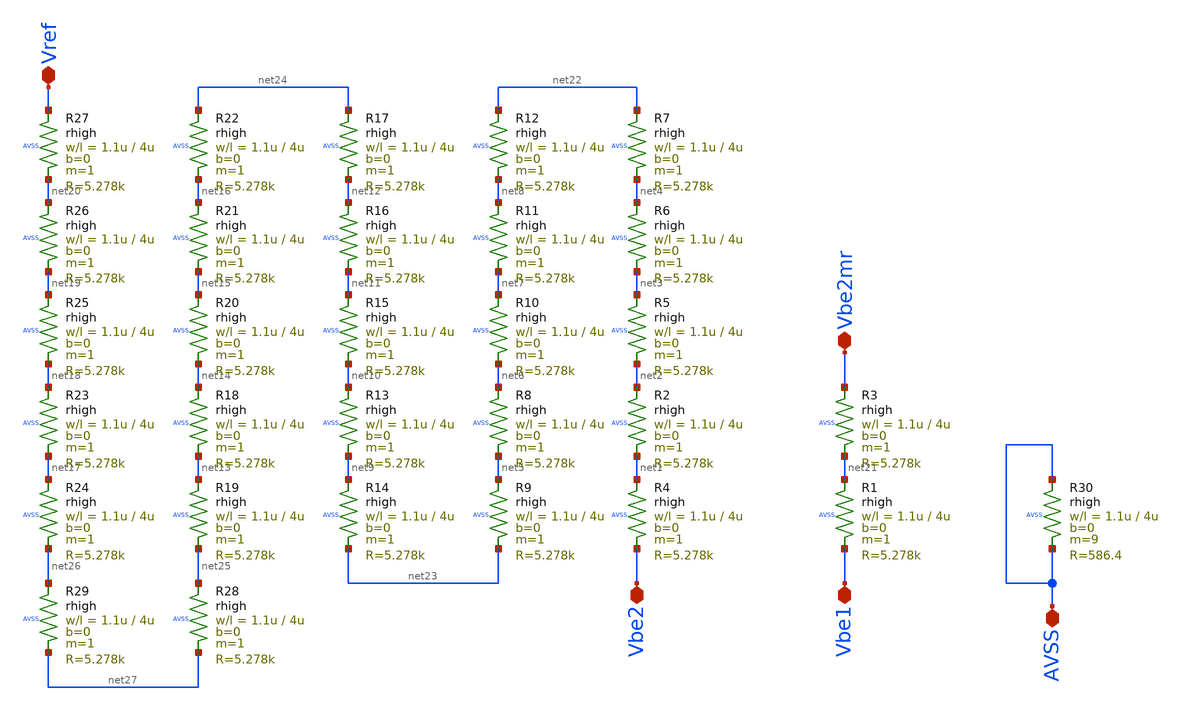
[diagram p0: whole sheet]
** sch_path: xschem/sg13cmos5l_srout_tinybgr_res.sch
**.subckt sg13cmos5l_srout_tinybgr_res Vbe1 Vbe2 AVSS Vbe2mr Vref
*.iopin Vbe1
*.iopin Vbe2
*.iopin AVSS
*.iopin Vbe2mr
*.iopin Vref
XR3 Vbe2mr net21 AVSS rhigh w=1.1u l=4u m=1 b=0 mm_ok=1
XR1 net21 Vbe1 AVSS rhigh w=1.1u l=4u m=1 b=0 mm_ok=1
XR2 net2 net1 AVSS rhigh w=1.1u l=4u m=1 b=0 mm_ok=1
XR4 net1 Vbe2 AVSS rhigh w=1.1u l=4u m=1 b=0 mm_ok=1
XR5 net3 net2 AVSS rhigh w=1.1u l=4u m=1 b=0 mm_ok=1
XR6 net4 net3 AVSS rhigh w=1.1u l=4u m=1 b=0 mm_ok=1
XR7 net22 net4 AVSS rhigh w=1.1u l=4u m=1 b=0 mm_ok=1
XR8 net6 net5 AVSS rhigh w=1.1u l=4u m=1 b=0 mm_ok=1
XR9 net5 net23 AVSS rhigh w=1.1u l=4u m=1 b=0 mm_ok=1
XR10 net7 net6 AVSS rhigh w=1.1u l=4u m=1 b=0 mm_ok=1
XR11 net8 net7 AVSS rhigh w=1.1u l=4u m=1 b=0 mm_ok=1
XR12 net22 net8 AVSS rhigh w=1.1u l=4u m=1 b=0 mm_ok=1
XR13 net10 net9 AVSS rhigh w=1.1u l=4u m=1 b=0 mm_ok=1
XR14 net9 net23 AVSS rhigh w=1.1u l=4u m=1 b=0 mm_ok=1
XR15 net11 net10 AVSS rhigh w=1.1u l=4u m=1 b=0 mm_ok=1
XR16 net12 net11 AVSS rhigh w=1.1u l=4u m=1 b=0 mm_ok=1
XR17 net24 net12 AVSS rhigh w=1.1u l=4u m=1 b=0 mm_ok=1
XR18 net14 net13 AVSS rhigh w=1.1u l=4u m=1 b=0 mm_ok=1
XR19 net13 net25 AVSS rhigh w=1.1u l=4u m=1 b=0 mm_ok=1
XR20 net15 net14 AVSS rhigh w=1.1u l=4u m=1 b=0 mm_ok=1
XR21 net16 net15 AVSS rhigh w=1.1u l=4u m=1 b=0 mm_ok=1
XR22 net24 net16 AVSS rhigh w=1.1u l=4u m=1 b=0 mm_ok=1
XR23 net18 net17 AVSS rhigh w=1.1u l=4u m=1 b=0 mm_ok=1
XR24 net17 net26 AVSS rhigh w=1.1u l=4u m=1 b=0 mm_ok=1
XR25 net19 net18 AVSS rhigh w=1.1u l=4u m=1 b=0 mm_ok=1
XR26 net20 net19 AVSS rhigh w=1.1u l=4u m=1 b=0 mm_ok=1
XR27 Vref net20 AVSS rhigh w=1.1u l=4u m=1 b=0 mm_ok=1
XR28 net25 net27 AVSS rhigh w=1.1u l=4u m=1 b=0 mm_ok=1
XR29 net26 net27 AVSS rhigh w=1.1u l=4u m=1 b=0 mm_ok=1
XR30 AVSS AVSS AVSS rhigh w=1.1u l=4u m=9 b=0 mm_ok=1
**.ends
.end
